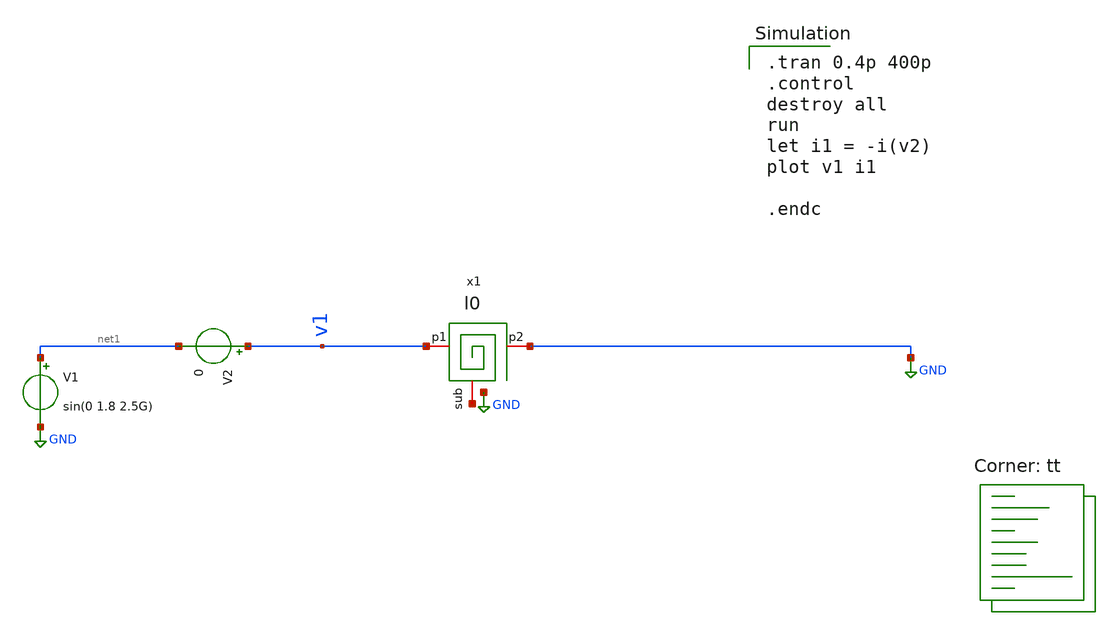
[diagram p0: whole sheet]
** sch_path: examples/sq_1nH_2.5GHz/xschem/tb-tran.sch
**.subckt tb-tran
V1 net1 GND sin(0 1.8 2.5G)
V2 v1 net1 0
x1 v1 GND net2 l0
**** begin user architecture code

.tran 0.4p 400p
.control
destroy all
run
let i1 = -i(v2)
plot v1 i1

.endc

.lib $::SKYWATER_MODELS/sky130.lib.spice tt
**** end user architecture code
**.ends

* expanding   symbol:  /foss/designs/asitic-example/examples/sq_1nH_2.5GHz/xschem/l0.sym # of pins=3
** sym_path: examples/sq_1nH_2.5GHz/xschem/l0.sym
** sch_path: examples/sq_1nH_2.5GHz/xschem/l0.sch
.subckt l0 p1 p2 sub
*.iopin sub
*.iopin p1
*.iopin p2
R net2 p2 2.857 m=1
L p1 net2 1.006n m=1
Rs1 net1 sub 27.37 m=1
Cs1 p1 net1 33.97f m=1
Cs2 p2 net3 36.78f m=1
Rs2 net3 sub -9 m=1
.ends

.GLOBAL GND
.end
